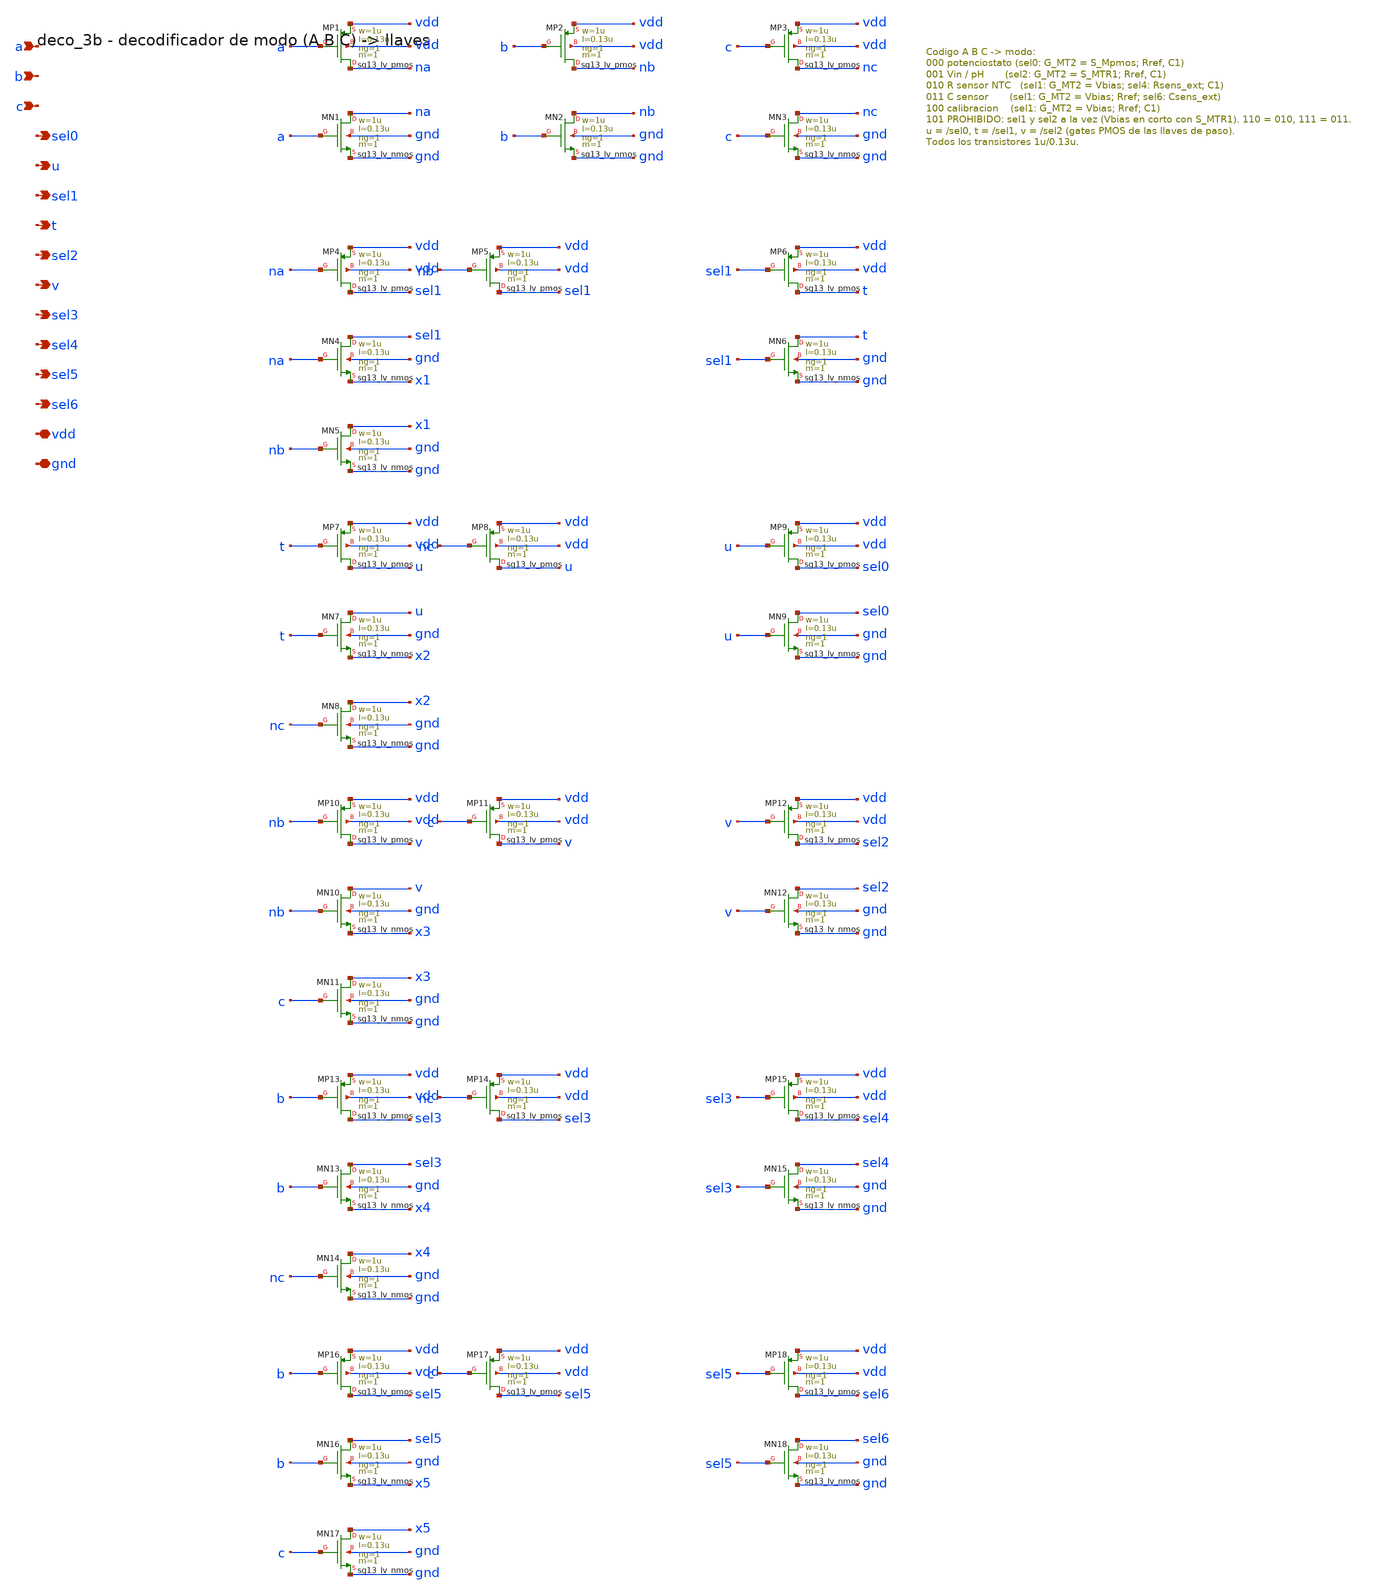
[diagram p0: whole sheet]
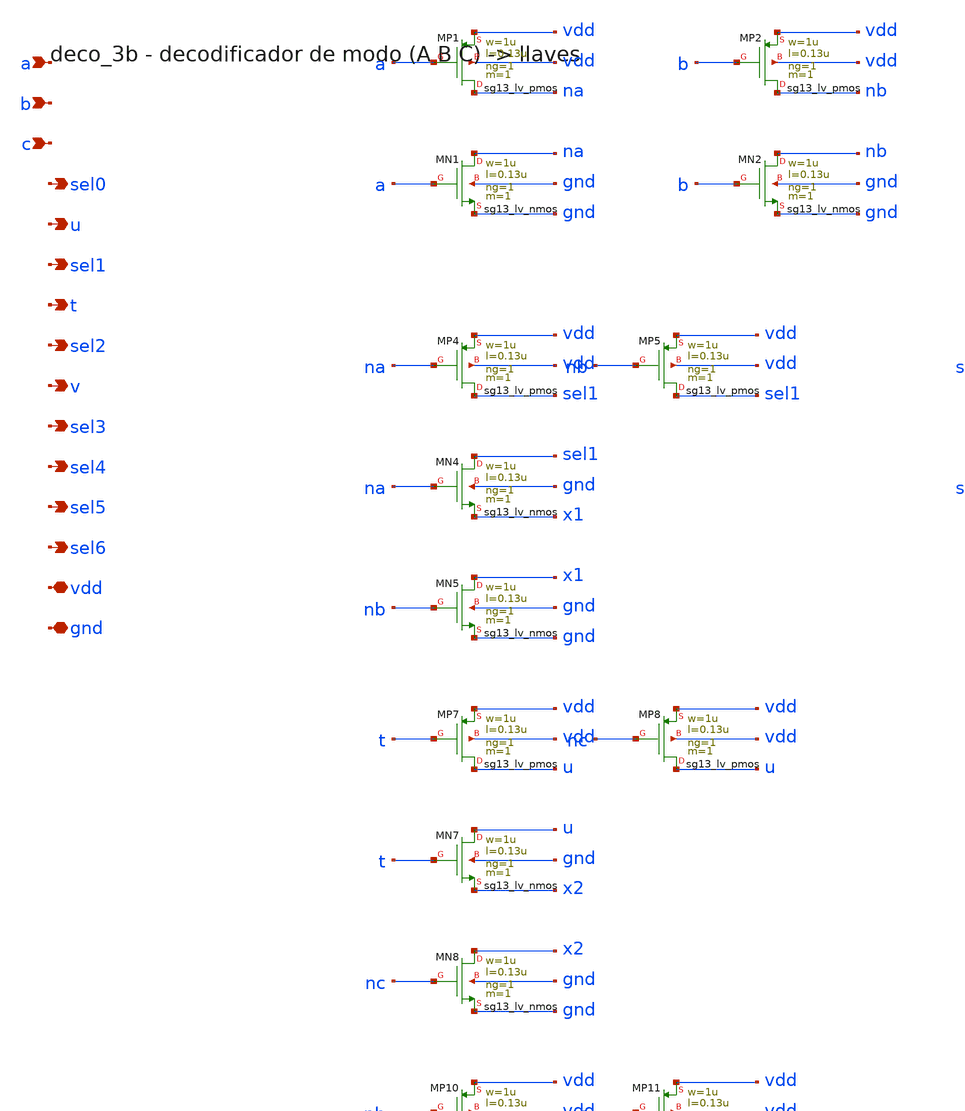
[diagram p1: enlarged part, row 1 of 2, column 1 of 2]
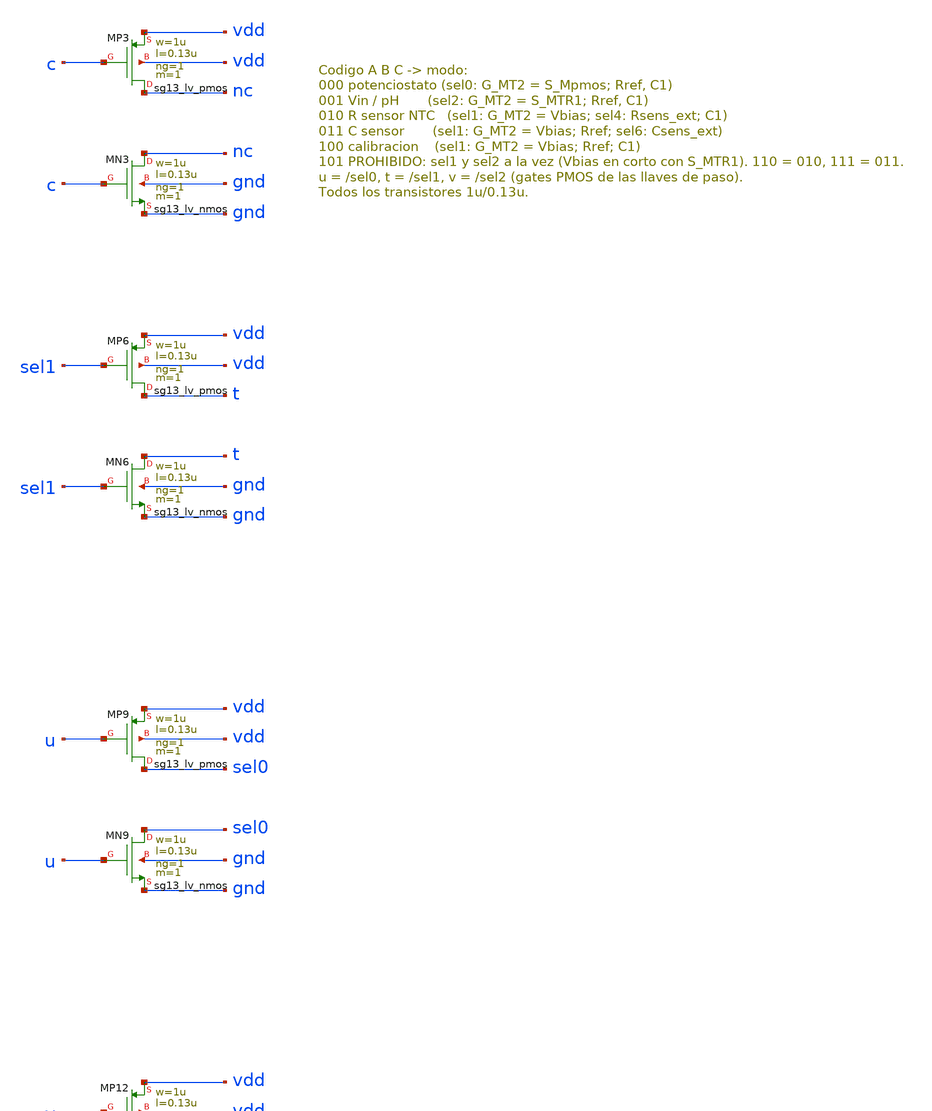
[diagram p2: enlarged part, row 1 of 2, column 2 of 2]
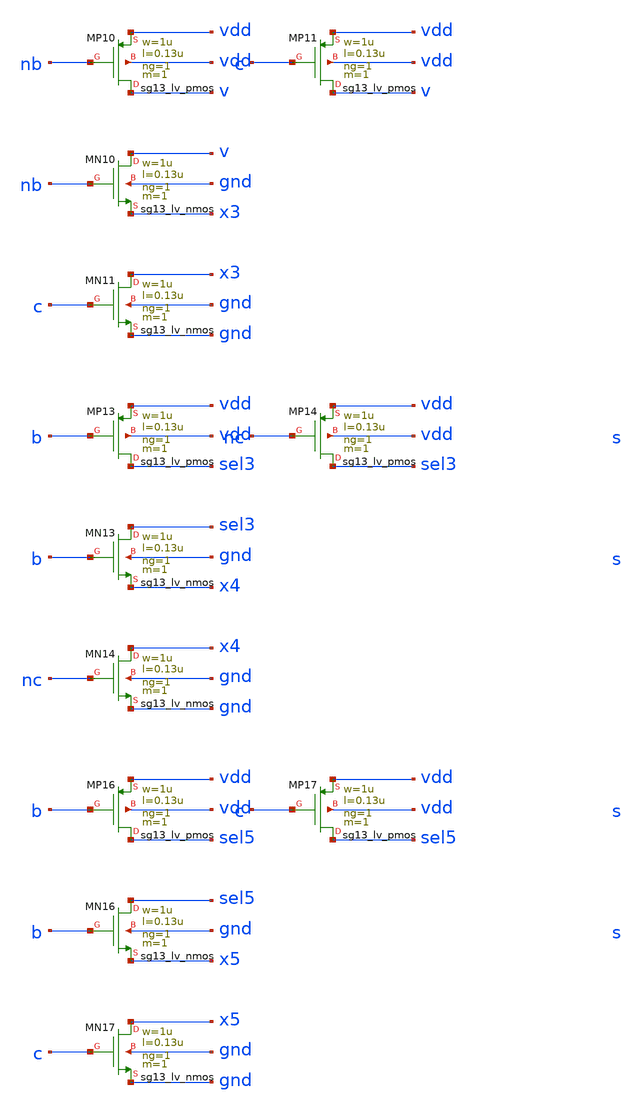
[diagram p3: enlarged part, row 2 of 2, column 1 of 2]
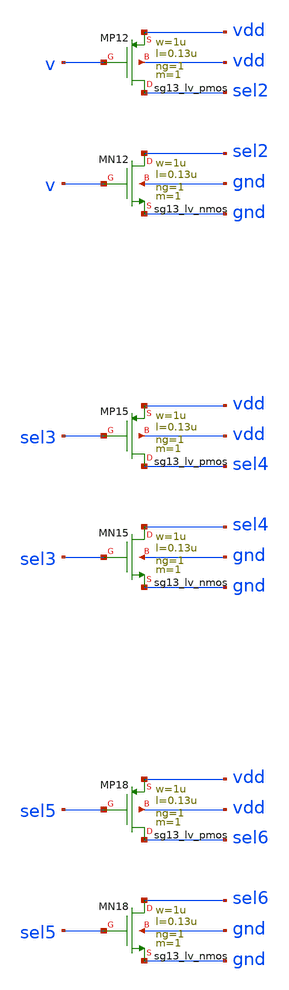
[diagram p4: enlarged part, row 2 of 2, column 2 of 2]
** sch_path: Enfoque_B/xschem/celdas/deco_3b.sch
**.subckt deco_3b a b c sel0 u sel1 t sel2 v sel3 sel4 sel5 sel6 vdd gnd
*.ipin a
*.ipin b
*.ipin c
*.opin sel0
*.opin u
*.opin sel1
*.opin t
*.opin sel2
*.opin v
*.opin sel3
*.opin sel4
*.opin sel5
*.opin sel6
*.iopin vdd
*.iopin gnd
XMP1 na a vdd vdd sg13_lv_pmos w=1u l=0.13u ng=1 m=1 mm_ok=1
XMN1 na a gnd gnd sg13_lv_nmos w=1u l=0.13u ng=1 m=1 mm_ok=1
XMP2 nb b vdd vdd sg13_lv_pmos w=1u l=0.13u ng=1 m=1 mm_ok=1
XMN2 nb b gnd gnd sg13_lv_nmos w=1u l=0.13u ng=1 m=1 mm_ok=1
XMP3 nc c vdd vdd sg13_lv_pmos w=1u l=0.13u ng=1 m=1 mm_ok=1
XMN3 nc c gnd gnd sg13_lv_nmos w=1u l=0.13u ng=1 m=1 mm_ok=1
XMP4 sel1 na vdd vdd sg13_lv_pmos w=1u l=0.13u ng=1 m=1 mm_ok=1
XMP5 sel1 nb vdd vdd sg13_lv_pmos w=1u l=0.13u ng=1 m=1 mm_ok=1
XMN4 sel1 na x1 gnd sg13_lv_nmos w=1u l=0.13u ng=1 m=1 mm_ok=1
XMN5 x1 nb gnd gnd sg13_lv_nmos w=1u l=0.13u ng=1 m=1 mm_ok=1
XMP6 t sel1 vdd vdd sg13_lv_pmos w=1u l=0.13u ng=1 m=1 mm_ok=1
XMN6 t sel1 gnd gnd sg13_lv_nmos w=1u l=0.13u ng=1 m=1 mm_ok=1
XMP7 u t vdd vdd sg13_lv_pmos w=1u l=0.13u ng=1 m=1 mm_ok=1
XMP8 u nc vdd vdd sg13_lv_pmos w=1u l=0.13u ng=1 m=1 mm_ok=1
XMN7 u t x2 gnd sg13_lv_nmos w=1u l=0.13u ng=1 m=1 mm_ok=1
XMN8 x2 nc gnd gnd sg13_lv_nmos w=1u l=0.13u ng=1 m=1 mm_ok=1
XMP9 sel0 u vdd vdd sg13_lv_pmos w=1u l=0.13u ng=1 m=1 mm_ok=1
XMN9 sel0 u gnd gnd sg13_lv_nmos w=1u l=0.13u ng=1 m=1 mm_ok=1
XMP10 v nb vdd vdd sg13_lv_pmos w=1u l=0.13u ng=1 m=1 mm_ok=1
XMP11 v c vdd vdd sg13_lv_pmos w=1u l=0.13u ng=1 m=1 mm_ok=1
XMN10 v nb x3 gnd sg13_lv_nmos w=1u l=0.13u ng=1 m=1 mm_ok=1
XMN11 x3 c gnd gnd sg13_lv_nmos w=1u l=0.13u ng=1 m=1 mm_ok=1
XMP12 sel2 v vdd vdd sg13_lv_pmos w=1u l=0.13u ng=1 m=1 mm_ok=1
XMN12 sel2 v gnd gnd sg13_lv_nmos w=1u l=0.13u ng=1 m=1 mm_ok=1
XMP13 sel3 b vdd vdd sg13_lv_pmos w=1u l=0.13u ng=1 m=1 mm_ok=1
XMP14 sel3 nc vdd vdd sg13_lv_pmos w=1u l=0.13u ng=1 m=1 mm_ok=1
XMN13 sel3 b x4 gnd sg13_lv_nmos w=1u l=0.13u ng=1 m=1 mm_ok=1
XMN14 x4 nc gnd gnd sg13_lv_nmos w=1u l=0.13u ng=1 m=1 mm_ok=1
XMP15 sel4 sel3 vdd vdd sg13_lv_pmos w=1u l=0.13u ng=1 m=1 mm_ok=1
XMN15 sel4 sel3 gnd gnd sg13_lv_nmos w=1u l=0.13u ng=1 m=1 mm_ok=1
XMP16 sel5 b vdd vdd sg13_lv_pmos w=1u l=0.13u ng=1 m=1 mm_ok=1
XMP17 sel5 c vdd vdd sg13_lv_pmos w=1u l=0.13u ng=1 m=1 mm_ok=1
XMN16 sel5 b x5 gnd sg13_lv_nmos w=1u l=0.13u ng=1 m=1 mm_ok=1
XMN17 x5 c gnd gnd sg13_lv_nmos w=1u l=0.13u ng=1 m=1 mm_ok=1
XMP18 sel6 sel5 vdd vdd sg13_lv_pmos w=1u l=0.13u ng=1 m=1 mm_ok=1
XMN18 sel6 sel5 gnd gnd sg13_lv_nmos w=1u l=0.13u ng=1 m=1 mm_ok=1
**.ends
.end
